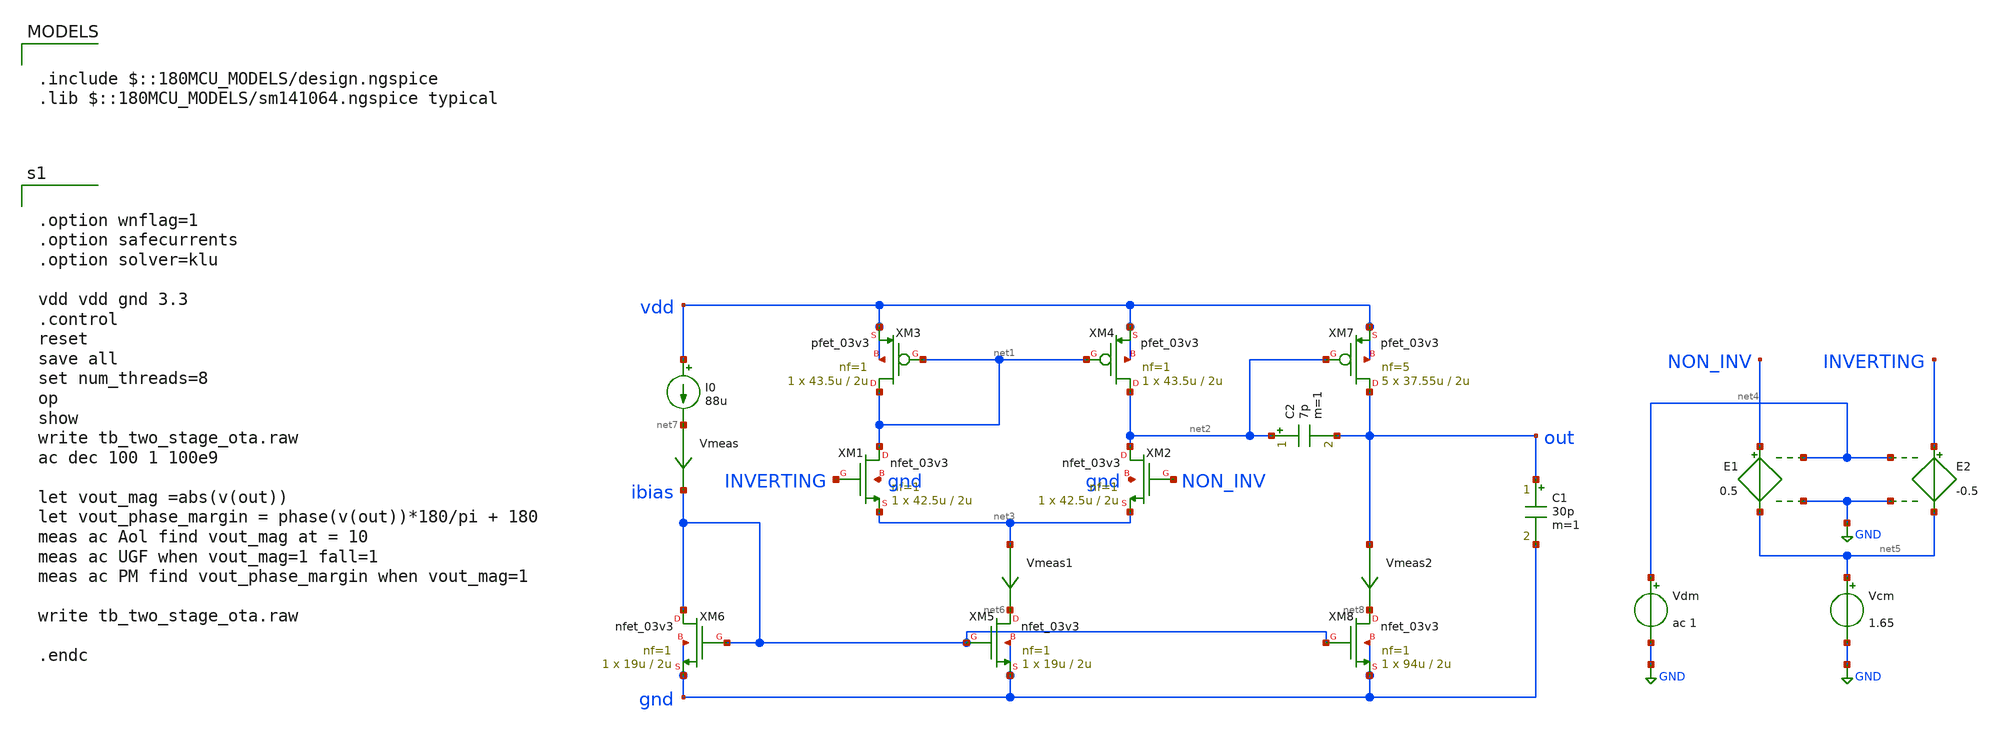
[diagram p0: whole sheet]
** sch_path: designs/libs/core_analog/two_stage_ota/two_stage_ota.sch
**.subckt two_stage_ota
XM1 net1 INVERTING net3 gnd nfet_03v3 L=2u W=42.5u nf=1 ad='int((nf+1)/2) * W/nf * 0.18u' as='int((nf+2)/2) * W/nf * 0.18u'
+ pd='2*int((nf+1)/2) * (W/nf + 0.18u)' ps='2*int((nf+2)/2) * (W/nf + 0.18u)' nrd='0.18u / W' nrs='0.18u / W'
+ sa=0 sb=0 sd=0 m=1
XM3 net1 net1 vdd vdd pfet_03v3 L=2u W=43.5u nf=1 ad='int((nf+1)/2) * W/nf * 0.18u' as='int((nf+2)/2) * W/nf * 0.18u'
+ pd='2*int((nf+1)/2) * (W/nf + 0.18u)' ps='2*int((nf+2)/2) * (W/nf + 0.18u)' nrd='0.18u / W' nrs='0.18u / W'
+ sa=0 sb=0 sd=0 m=1
XM5 net6 ibias gnd gnd nfet_03v3 L=2u W=19u nf=1 ad='int((nf+1)/2) * W/nf * 0.18u' as='int((nf+2)/2) * W/nf * 0.18u'
+ pd='2*int((nf+1)/2) * (W/nf + 0.18u)' ps='2*int((nf+2)/2) * (W/nf + 0.18u)' nrd='0.18u / W' nrs='0.18u / W'
+ sa=0 sb=0 sd=0 m=1
XM6 ibias ibias gnd gnd nfet_03v3 L=2u W=19u nf=1 ad='int((nf+1)/2) * W/nf * 0.18u' as='int((nf+2)/2) * W/nf * 0.18u'
+ pd='2*int((nf+1)/2) * (W/nf + 0.18u)' ps='2*int((nf+2)/2) * (W/nf + 0.18u)' nrd='0.18u / W' nrs='0.18u / W'
+ sa=0 sb=0 sd=0 m=1
I0 vdd net7 88u
XM7 out net2 vdd vdd pfet_03v3 L=2u W=37.55u nf=5 ad='int((nf+1)/2) * W/nf * 0.18u' as='int((nf+2)/2) * W/nf * 0.18u'
+ pd='2*int((nf+1)/2) * (W/nf + 0.18u)' ps='2*int((nf+2)/2) * (W/nf + 0.18u)' nrd='0.18u / W' nrs='0.18u / W'
+ sa=0 sb=0 sd=0 m=5
XM8 net8 ibias gnd gnd nfet_03v3 L=2u W=94u nf=1 ad='int((nf+1)/2) * W/nf * 0.18u' as='int((nf+2)/2) * W/nf * 0.18u'
+ pd='2*int((nf+1)/2) * (W/nf + 0.18u)' ps='2*int((nf+2)/2) * (W/nf + 0.18u)' nrd='0.18u / W' nrs='0.18u / W'
+ sa=0 sb=0 sd=0 m=1
C1 out gnd 30p m=1
C2 net2 out 7p m=1
XM2 net2 NON_INV net3 gnd nfet_03v3 L=2u W=42.5u nf=1 ad='int((nf+1)/2) * W/nf * 0.18u' as='int((nf+2)/2) * W/nf * 0.18u'
+ pd='2*int((nf+1)/2) * (W/nf + 0.18u)' ps='2*int((nf+2)/2) * (W/nf + 0.18u)' nrd='0.18u / W' nrs='0.18u / W'
+ sa=0 sb=0 sd=0 m=1
XM4 net2 net1 vdd vdd pfet_03v3 L=2u W=43.5u nf=1 ad='int((nf+1)/2) * W/nf * 0.18u' as='int((nf+2)/2) * W/nf * 0.18u'
+ pd='2*int((nf+1)/2) * (W/nf + 0.18u)' ps='2*int((nf+2)/2) * (W/nf + 0.18u)' nrd='0.18u / W' nrs='0.18u / W'
+ sa=0 sb=0 sd=0 m=1
E1 NON_INV net5 net4 GND 0.5
E2 INVERTING net5 net4 GND -0.5
Vdm net4 GND ac 1
Vcm net5 GND 1.65
Vmeas net7 ibias 0
.save i(vmeas)
Vmeas1 net3 net6 0
.save i(vmeas1)
Vmeas2 out net8 0
.save i(vmeas2)
**** begin user architecture code


.option wnflag=1
.option safecurrents
.option solver=klu

vdd vdd gnd 3.3
.control
reset
save all
set num_threads=8
op
show
write tb_two_stage_ota.raw
ac dec 100 1 100e9

let vout_mag =abs(v(out))
let vout_phase_margin = phase(v(out))*180/pi + 180
meas ac Aol find vout_mag at = 10
meas ac UGF when vout_mag=1 fall=1
meas ac PM find vout_phase_margin when vout_mag=1

write tb_two_stage_ota.raw

.endc



.include $::180MCU_MODELS/design.ngspice
.lib $::180MCU_MODELS/sm141064.ngspice typical

**** end user architecture code
**.ends
.GLOBAL GND
.end
